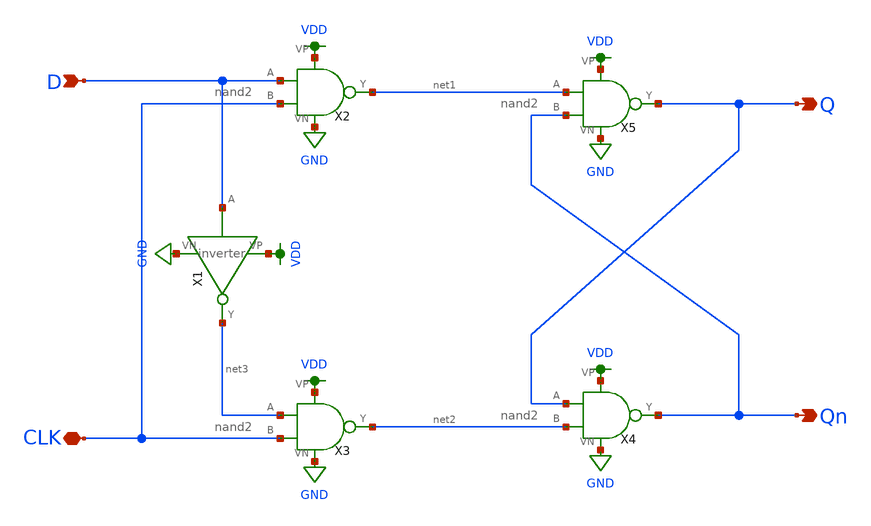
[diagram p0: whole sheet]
** sch_path: schematic/dff.sch
**.subckt dff D CLK Qn Q
*.ipin D
*.iopin CLK
*.opin Qn
*.opin Q
X2 D CLK net1 VDD GND nand2
X3 net3 CLK net2 VDD GND nand2
X4 Q net2 Qn VDD GND nand2
X5 net1 Qn Q VDD GND nand2
X1 D net3 VDD GND inverter
**.ends

* expanding   symbol:  /home/madvlsi/Documents/MADVLSI-Final_Project/schematic/nand2.sym # of pins=5
** sym_path: schematic/nand2.sym
** sch_path: schematic/nand2.sch
.subckt nand2 A B Y VP VN
*.ipin A
*.opin Y
*.ipin B
*.iopin VP
*.iopin VP
*.iopin VN
*.iopin VN
XM1 Y A VP VP sky130_fd_pr__pfet_01v8 L=0.15 W=2 nf=1 ad='int((nf+1)/2) * W/nf * 0.29' as='int((nf+2)/2) * W/nf * 0.29'
+ pd='2*int((nf+1)/2) * (W/nf + 0.29)' ps='2*int((nf+2)/2) * (W/nf + 0.29)' nrd='0.29 / W' nrs='0.29 / W'
+ sa=0 sb=0 sd=0 mult=1 m=1
XM2 VP B Y VP sky130_fd_pr__pfet_01v8 L=0.15 W=2 nf=1 ad='int((nf+1)/2) * W/nf * 0.29' as='int((nf+2)/2) * W/nf * 0.29'
+ pd='2*int((nf+1)/2) * (W/nf + 0.29)' ps='2*int((nf+2)/2) * (W/nf + 0.29)' nrd='0.29 / W' nrs='0.29 / W'
+ sa=0 sb=0 sd=0 mult=1 m=1
XM3 net1 B Y VN sky130_fd_pr__nfet_01v8 L=0.15 W=2 nf=1 ad='int((nf+1)/2) * W/nf * 0.29' as='int((nf+2)/2) * W/nf * 0.29'
+ pd='2*int((nf+1)/2) * (W/nf + 0.29)' ps='2*int((nf+2)/2) * (W/nf + 0.29)' nrd='0.29 / W' nrs='0.29 / W'
+ sa=0 sb=0 sd=0 mult=1 m=1
XM4 net1 A VN VN sky130_fd_pr__nfet_01v8 L=0.15 W=2 nf=1 ad='int((nf+1)/2) * W/nf * 0.29' as='int((nf+2)/2) * W/nf * 0.29'
+ pd='2*int((nf+1)/2) * (W/nf + 0.29)' ps='2*int((nf+2)/2) * (W/nf + 0.29)' nrd='0.29 / W' nrs='0.29 / W'
+ sa=0 sb=0 sd=0 mult=1 m=1
.ends


* expanding   symbol:  /home/madvlsi/Documents/MADVLSI-Final_Project/schematic/inverter.sym # of
*+ pins=4
** sym_path: schematic/inverter.sym
** sch_path: schematic/inverter.sch
.subckt inverter A Y VP VN
*.opin Y
*.ipin A
*.iopin VP
*.iopin VN
XM3 Y A VP VDD sky130_fd_pr__pfet_01v8 L={Lp} W={Wp} nf=1 ad='int((nf+1)/2) * W/nf * 0.29' as='int((nf+2)/2) * W/nf * 0.29'
+ pd='2*int((nf+1)/2) * (W/nf + 0.29)' ps='2*int((nf+2)/2) * (W/nf + 0.29)' nrd='0.29 / W' nrs='0.29 / W'
+ sa=0 sb=0 sd=0 mult=1 m=1
XM4 Y A VP VDD sky130_fd_pr__pfet_01v8 L={Lp} W={Wp} nf=1 ad='int((nf+1)/2) * W/nf * 0.29' as='int((nf+2)/2) * W/nf * 0.29'
+ pd='2*int((nf+1)/2) * (W/nf + 0.29)' ps='2*int((nf+2)/2) * (W/nf + 0.29)' nrd='0.29 / W' nrs='0.29 / W'
+ sa=0 sb=0 sd=0 mult=1 m=1
XM5 Y A VN GND sky130_fd_pr__nfet_01v8 L={Lp} W={Wp} nf=1 ad='int((nf+1)/2) * W/nf * 0.29' as='int((nf+2)/2) * W/nf * 0.29'
+ pd='2*int((nf+1)/2) * (W/nf + 0.29)' ps='2*int((nf+2)/2) * (W/nf + 0.29)' nrd='0.29 / W' nrs='0.29 / W'
+ sa=0 sb=0 sd=0 mult=1 m=1
.ends

.GLOBAL VDD
.GLOBAL GND
.end
